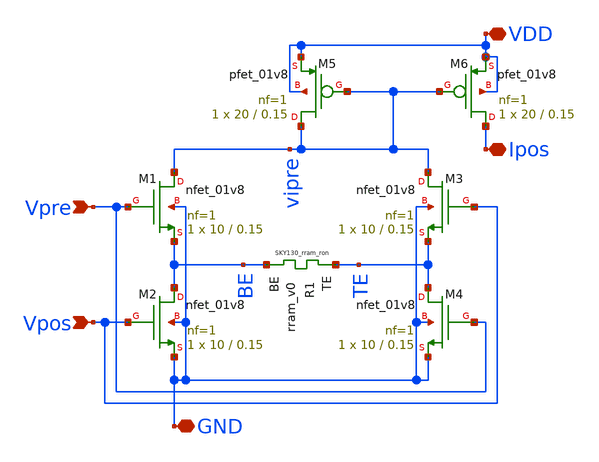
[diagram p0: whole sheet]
** sch_path: synapse/6T1R.sch
**.subckt 6T1R Vpre Vpos GND Ipos VDD
*.ipin Vpre
*.ipin Vpos
*.iopin GND
*.iopin Ipos
*.iopin VDD
XM1 vipre Vpre BE GND sky130_fd_pr__nfet_01v8 L=0.15 W=10 nf=1 ad='int((nf+1)/2) * W/nf * 0.29' as='int((nf+2)/2) * W/nf * 0.29'
+ pd='2*int((nf+1)/2) * (W/nf + 0.29)' ps='2*int((nf+2)/2) * (W/nf + 0.29)' nrd='0.29 / W' nrs='0.29 / W'
+ sa=0 sb=0 sd=0 mult=1 m=1
XR1 TE BE rram_v0
XM3 vipre Vpos TE GND sky130_fd_pr__nfet_01v8 L=0.15 W=10 nf=1 ad='int((nf+1)/2) * W/nf * 0.29' as='int((nf+2)/2) * W/nf * 0.29'
+ pd='2*int((nf+1)/2) * (W/nf + 0.29)' ps='2*int((nf+2)/2) * (W/nf + 0.29)' nrd='0.29 / W' nrs='0.29 / W'
+ sa=0 sb=0 sd=0 mult=1 m=1
XM6 Ipos vipre VDD VDD sky130_fd_pr__pfet_01v8 L=0.15 W=20 nf=1 ad='int((nf+1)/2) * W/nf * 0.29' as='int((nf+2)/2) * W/nf * 0.29'
+ pd='2*int((nf+1)/2) * (W/nf + 0.29)' ps='2*int((nf+2)/2) * (W/nf + 0.29)' nrd='0.29 / W' nrs='0.29 / W'
+ sa=0 sb=0 sd=0 mult=1 m=1
XM5 vipre vipre VDD VDD sky130_fd_pr__pfet_01v8 L=0.15 W=20 nf=1 ad='int((nf+1)/2) * W/nf * 0.29' as='int((nf+2)/2) * W/nf * 0.29'
+ pd='2*int((nf+1)/2) * (W/nf + 0.29)' ps='2*int((nf+2)/2) * (W/nf + 0.29)' nrd='0.29 / W' nrs='0.29 / W'
+ sa=0 sb=0 sd=0 mult=1 m=1
XM2 BE Vpos GND GND sky130_fd_pr__nfet_01v8 L=0.15 W=10 nf=1 ad='int((nf+1)/2) * W/nf * 0.29' as='int((nf+2)/2) * W/nf * 0.29'
+ pd='2*int((nf+1)/2) * (W/nf + 0.29)' ps='2*int((nf+2)/2) * (W/nf + 0.29)' nrd='0.29 / W' nrs='0.29 / W'
+ sa=0 sb=0 sd=0 mult=1 m=1
XM4 TE Vpre GND GND sky130_fd_pr__nfet_01v8 L=0.15 W=10 nf=1 ad='int((nf+1)/2) * W/nf * 0.29' as='int((nf+2)/2) * W/nf * 0.29'
+ pd='2*int((nf+1)/2) * (W/nf + 0.29)' ps='2*int((nf+2)/2) * (W/nf + 0.29)' nrd='0.29 / W' nrs='0.29 / W'
+ sa=0 sb=0 sd=0 mult=1 m=1
**.ends
.end
